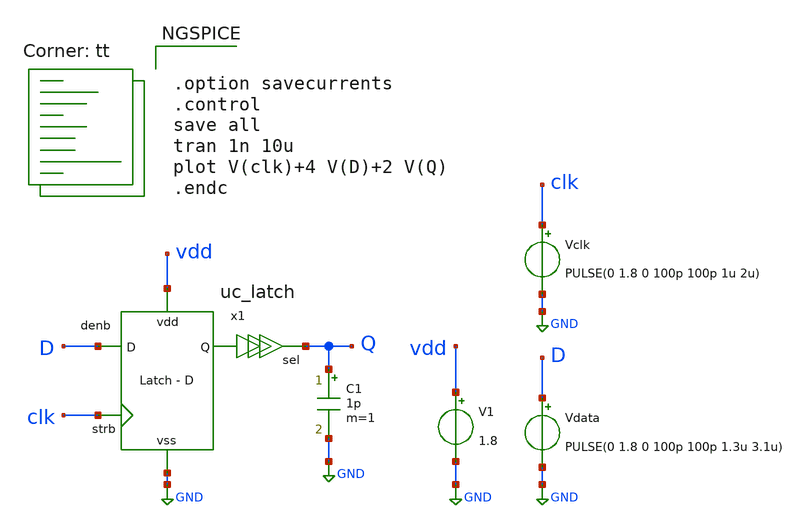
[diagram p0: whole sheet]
** sch_path: xschem/uc_latch/uc_latch_tb.sch
**.subckt uc_latch_tb
x1 vdd GND clk D Q uc_latch
Vclk clk GND PULSE(0 1.8 0 100p 100p 1u 2u)
Vdata D GND PULSE(0 1.8 0 100p 100p 1.3u 3.1u)
C1 Q GND 1p m=1
V1 vdd GND 1.8
**** begin user architecture code
.lib $::SKYWATER_MODELS/sky130.lib.spice tt


.option savecurrents
.control
save all
tran 1n 10u
plot V(clk)+4 V(D)+2 V(Q)
.endc


**** end user architecture code
**.ends
.GLOBAL GND
.end
